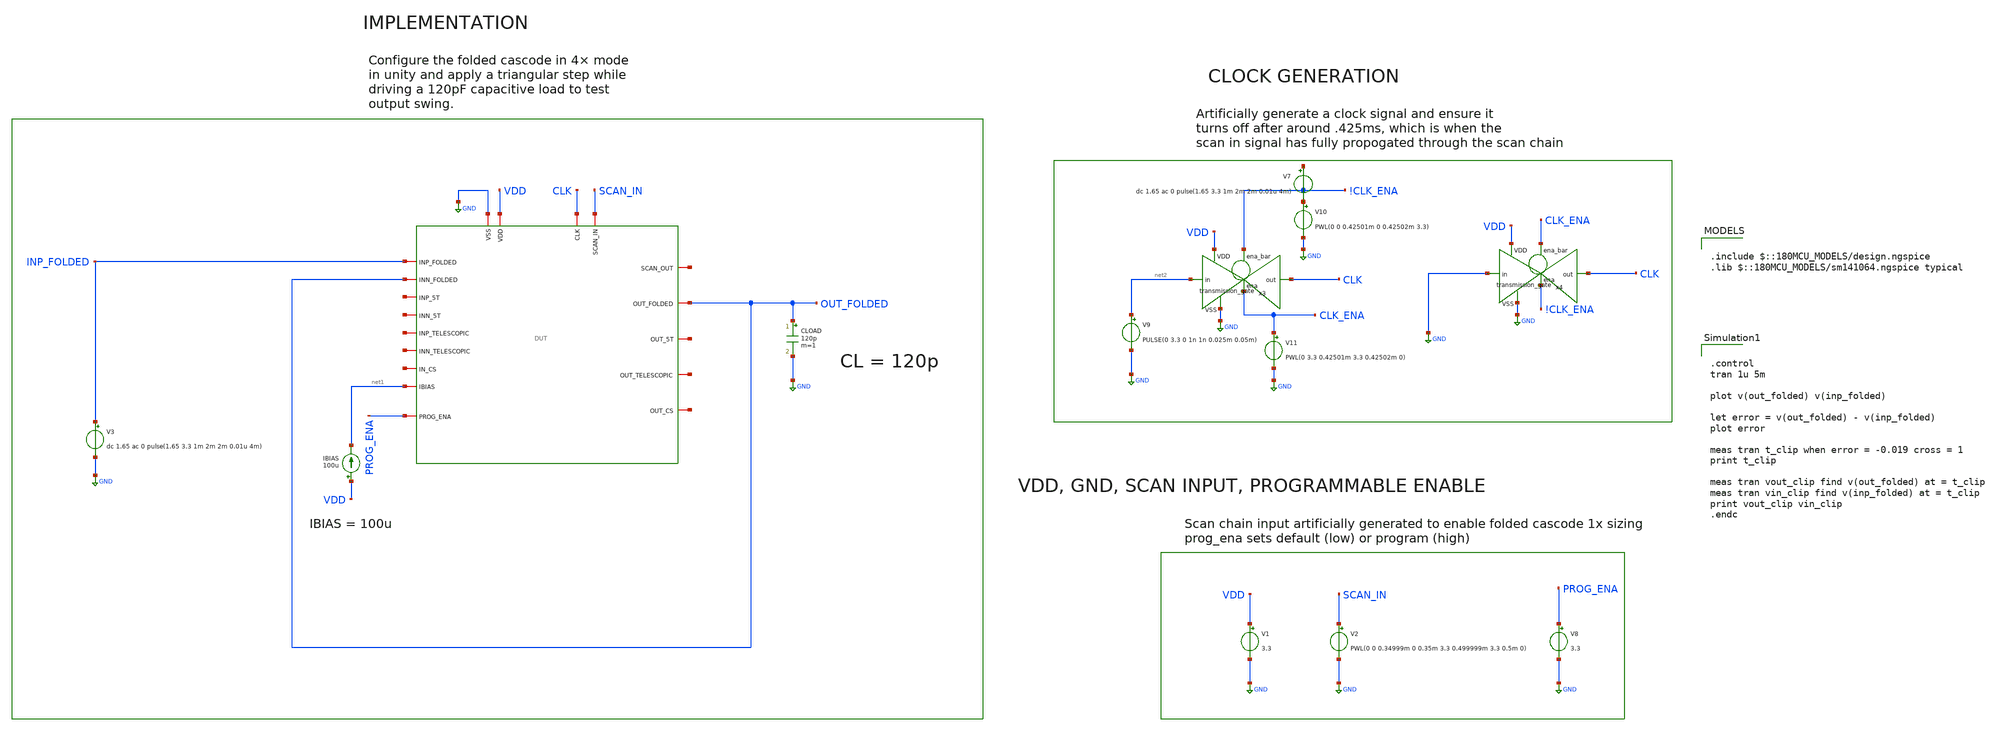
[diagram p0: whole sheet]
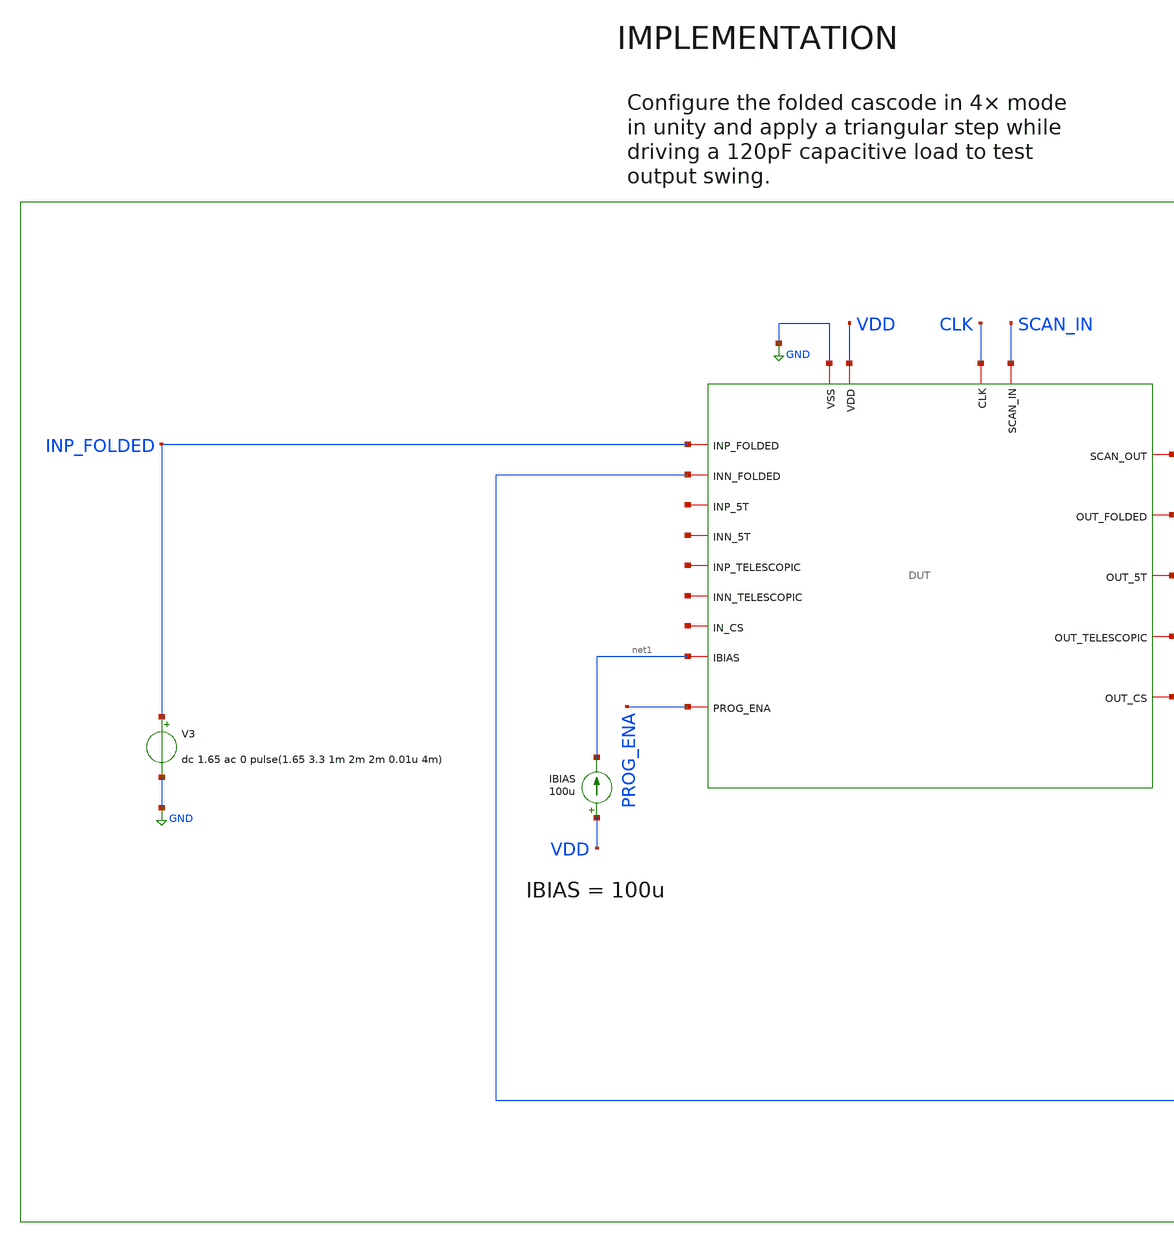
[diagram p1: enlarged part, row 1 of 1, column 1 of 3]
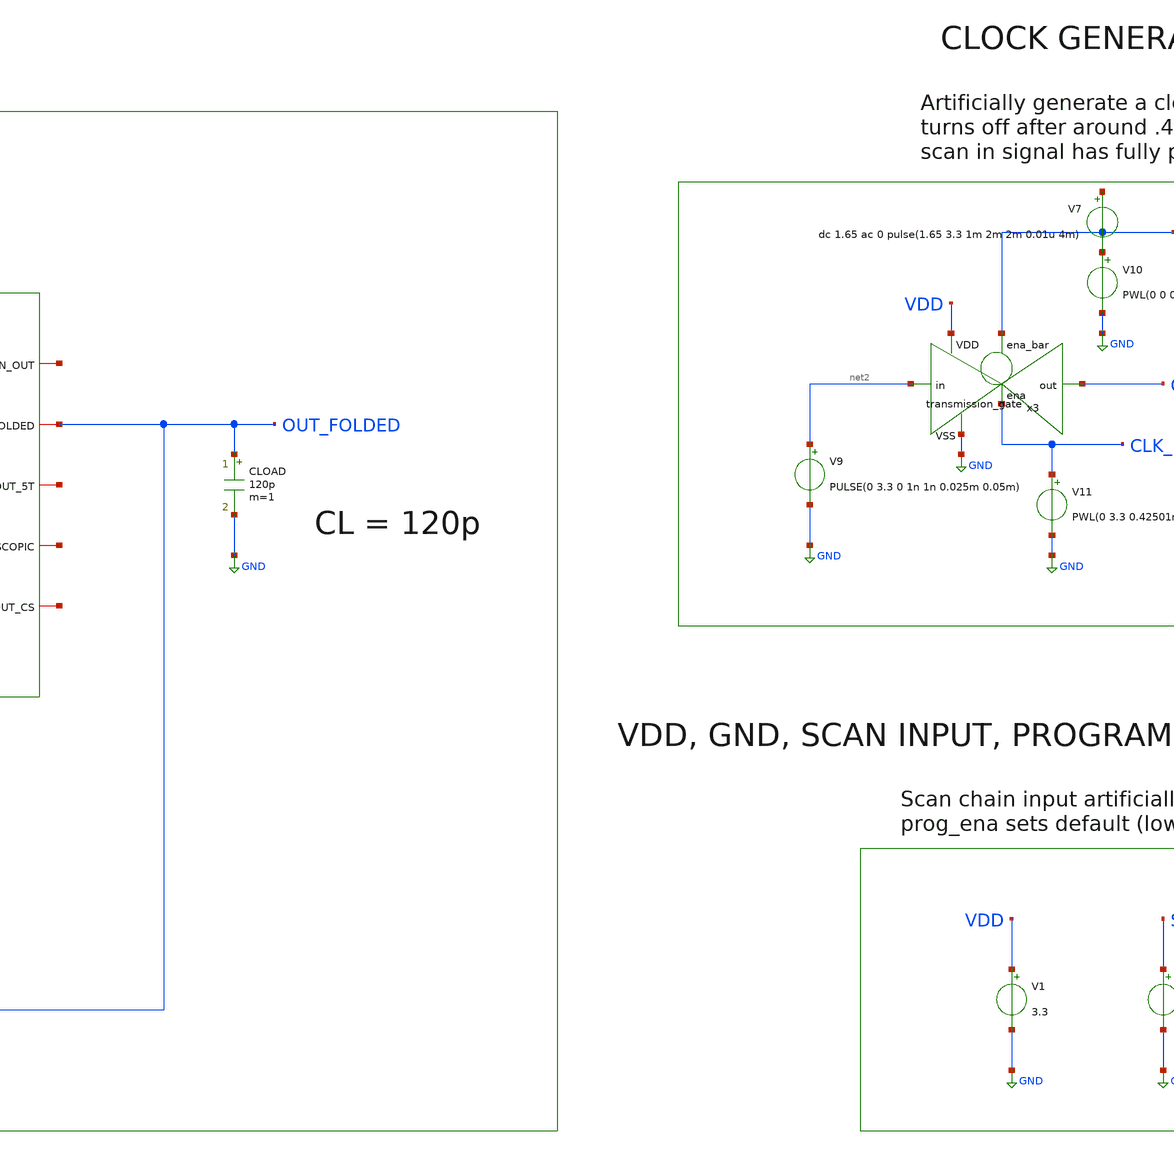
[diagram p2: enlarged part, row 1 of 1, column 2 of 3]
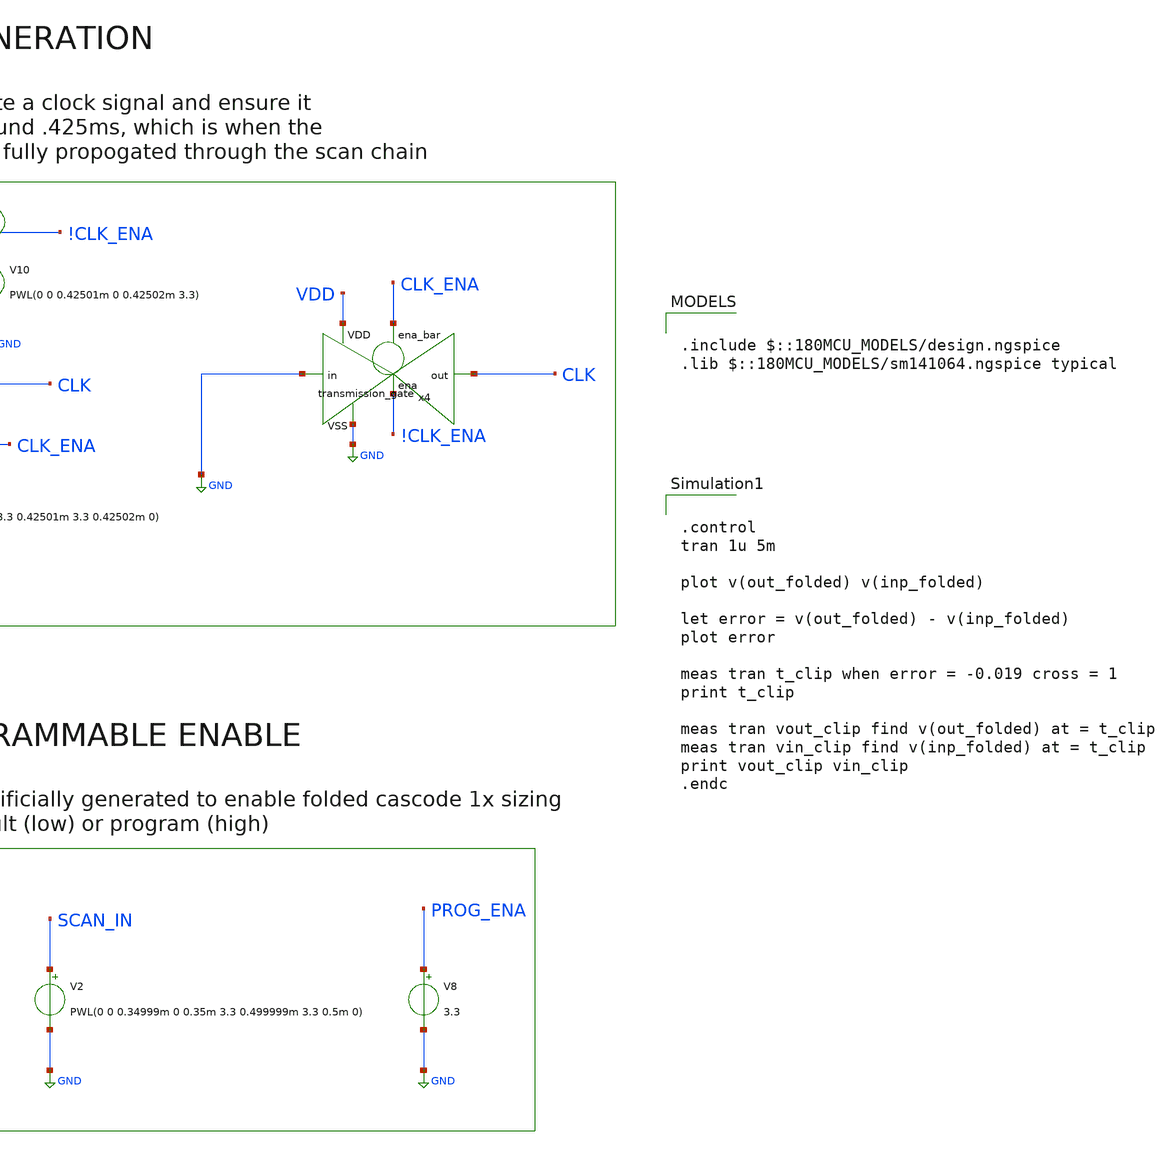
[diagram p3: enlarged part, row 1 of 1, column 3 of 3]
** sch_path: designs/libs/verification/ota_folded/4x_sizing/large_signal_upper_swing_tb.sch
**.subckt large_signal_upper_swing_tb
V1 VDD GND 3.3
IBIAS VDD net1 100u
CLOAD OUT_FOLDED GND 120p m=1
x1 CLK net3 SCAN_IN GND VDD OUT_FOLDED INP_FOLDED net4 net1 OUT_FOLDED net5 net6 net7 net8 net9
+ net10 net11 PROG_ENA DUT
V8 PROG_ENA GND 3.3
V9 net2 GND PULSE(0 3.3 0 1n 1n 0.025m 0.05m)
x3 !CLK_ENA VDD CLK net2 GND CLK_ENA transmission_gate
V10 !CLK_ENA GND PWL(0 0 0.42501m 0 0.42502m 3.3)
V11 CLK_ENA GND PWL(0 3.3 0.42501m 3.3 0.42502m 0)
x4 CLK_ENA VDD CLK GND GND !CLK_ENA transmission_gate
V2 SCAN_IN GND PWL(0 0 0.34999m 0 0.35m 3.3 0.499999m 3.3 0.5m 0)
V7 net12 !CLK_ENA dc 1.65 ac 0 pulse(1.65 3.3 1m 2m 2m 0.01u 4m)
V3 INP_FOLDED GND dc 1.65 ac 0 pulse(1.65 3.3 1m 2m 2m 0.01u 4m)
**** begin user architecture code

.include $::180MCU_MODELS/design.ngspice
.lib $::180MCU_MODELS/sm141064.ngspice typical



.control
tran 1u 5m

plot v(out_folded) v(inp_folded)

let error = v(out_folded) - v(inp_folded)
plot error

meas tran t_clip when error = -0.019 cross = 1
print t_clip

meas tran vout_clip find v(out_folded) at = t_clip
meas tran vin_clip find v(inp_folded) at = t_clip
print vout_clip vin_clip
.endc


**** end user architecture code
**.ends
.GLOBAL GND
.end
